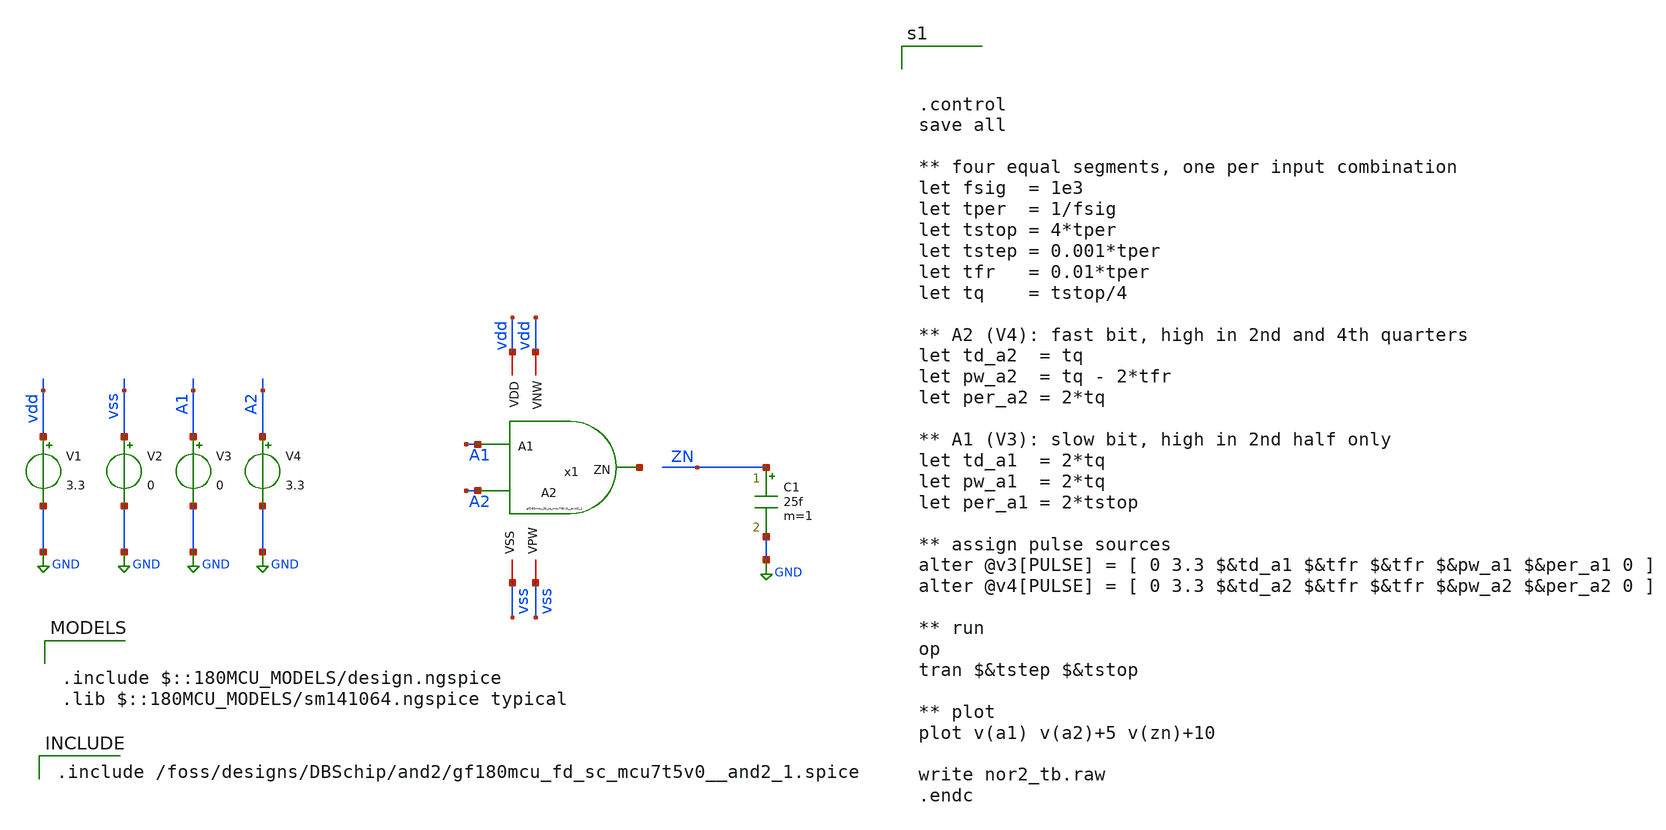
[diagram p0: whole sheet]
** sch_path: and2/and2_1_tb.sch
**.subckt and2_1_tb
V1 vdd GND 3.3
V2 vss GND 0
V3 A1 GND 0
V4 A2 GND 3.3
C1 ZN GND 25f m=1
x1 A1 A2 net1 vdd vdd vss vss gf180mcu_fd_sc_mcu7t5v0__and2_1
**** begin user architecture code

.include $::180MCU_MODELS/design.ngspice
.lib $::180MCU_MODELS/sm141064.ngspice typical


.include /foss/designs/DBSchip/and2/gf180mcu_fd_sc_mcu7t5v0__and2_1.spice




.control
save all

** four equal segments, one per input combination
let fsig  = 1e3
let tper  = 1/fsig
let tstop = 4*tper
let tstep = 0.001*tper
let tfr   = 0.01*tper
let tq    = tstop/4

** A2 (V4): fast bit, high in 2nd and 4th quarters
let td_a2  = tq
let pw_a2  = tq - 2*tfr
let per_a2 = 2*tq

** A1 (V3): slow bit, high in 2nd half only
let td_a1  = 2*tq
let pw_a1  = 2*tq
let per_a1 = 2*tstop

** assign pulse sources
alter @v3[PULSE] = [ 0 3.3 $&td_a1 $&tfr $&tfr $&pw_a1 $&per_a1 0 ]
alter @v4[PULSE] = [ 0 3.3 $&td_a2 $&tfr $&tfr $&pw_a2 $&per_a2 0 ]

** run
op
tran $&tstep $&tstop

** plot
plot v(a1) v(a2)+5 v(zn)+10

write nor2_tb.raw
.endc


**** end user architecture code
**.ends
.GLOBAL GND
.end
